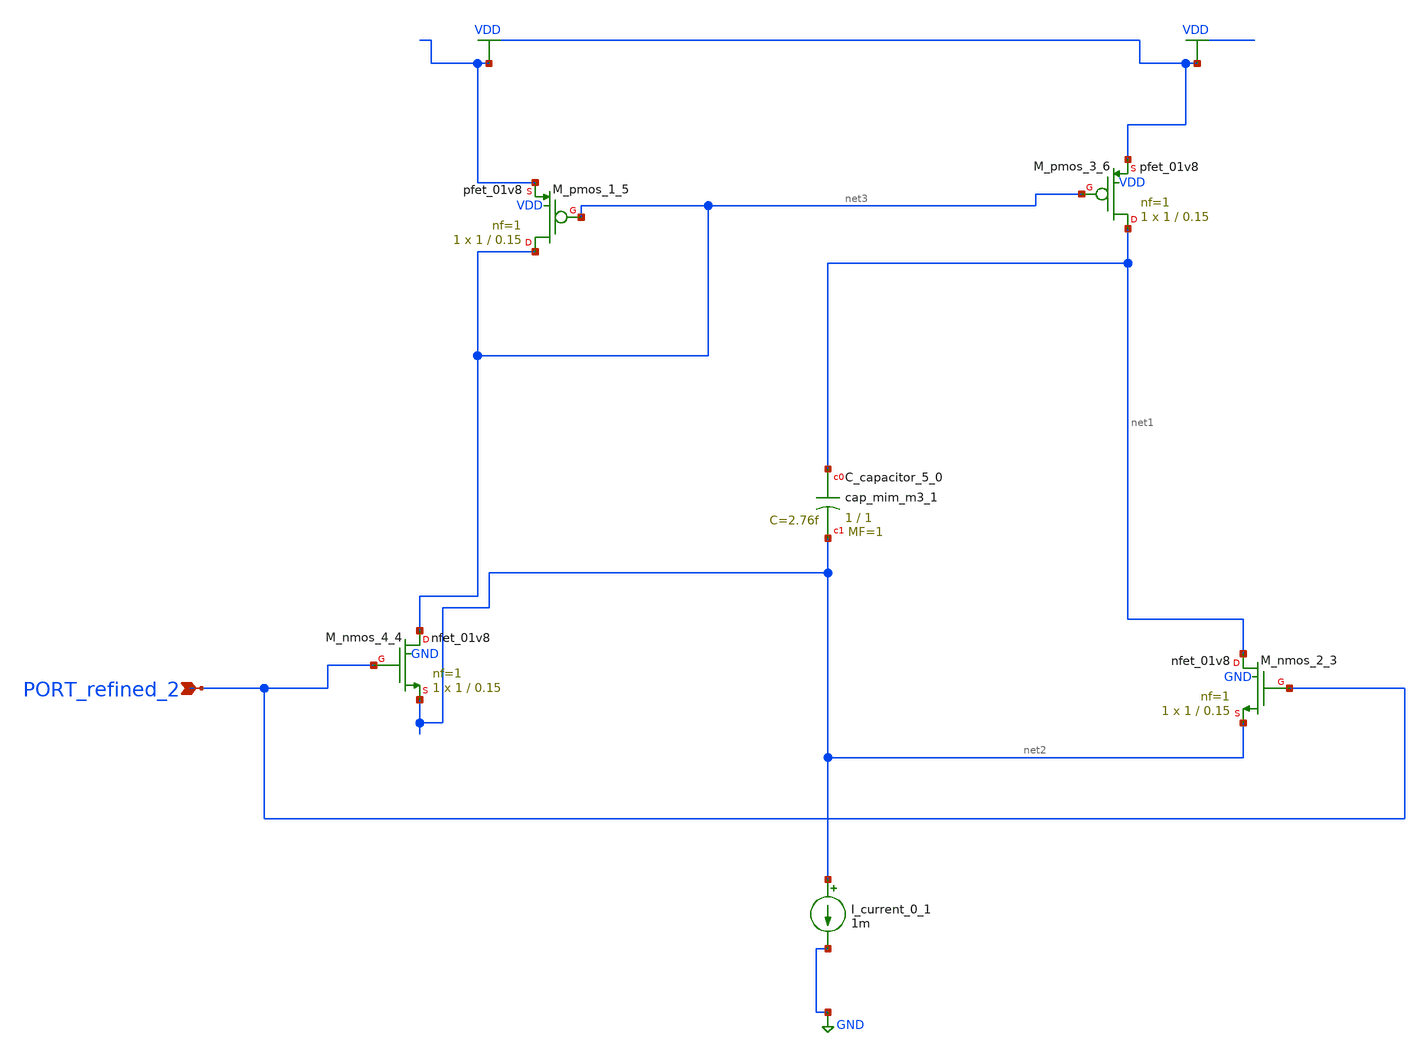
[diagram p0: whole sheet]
** sch_path: schematics/AMSNet/353.sch
**.subckt 353 PORT_refined_2
*.ipin PORT_refined_2
XC_capacitor_5_0 net1 net2 sky130_fd_pr__cap_mim_m3_1 W=1 L=1 MF=1 m=1
I_current_0_1 net2 GND 1m
XM_nmos_2_3 net1 PORT_refined_2 net2 GND sky130_fd_pr__nfet_01v8 L=0.15 W=1 nf=1 ad='int((1 + 1)/2) * 1 / 1 * 0.29'
+ as='int((1 + 2)/2) * 1 / 1 * 0.29' pd='2*int((1 + 1)/2) * (1 / 1 + 0.29)' ps='2*int((1 + 2)/2) * (1 / 1 + 0.29)'
+ nrd='0.29 / 1 ' nrs='0.29 / 1 ' sa=0 sb=0 sd=0 mult=1 m=1
XM_nmos_4_4 net3 PORT_refined_2 net2 GND sky130_fd_pr__nfet_01v8 L=0.15 W=1 nf=1 ad='int((1 + 1)/2) * 1 / 1 * 0.29'
+ as='int((1 + 2)/2) * 1 / 1 * 0.29' pd='2*int((1 + 1)/2) * (1 / 1 + 0.29)' ps='2*int((1 + 2)/2) * (1 / 1 + 0.29)'
+ nrd='0.29 / 1 ' nrs='0.29 / 1 ' sa=0 sb=0 sd=0 mult=1 m=1
XM_pmos_1_5 net3 net3 VDD VDD sky130_fd_pr__pfet_01v8 L=0.15 W=1 nf=1 ad='int((1 + 1)/2) * 1 / 1 * 0.29'
+ as='int((1 + 2)/2) * 1 / 1 * 0.29' pd='2*int((1 + 1)/2) * (1 / 1 + 0.29)' ps='2*int((1 + 2)/2) * (1 / 1 + 0.29)'
+ nrd='0.29 / 1 ' nrs='0.29 / 1 ' sa=0 sb=0 sd=0 mult=1 m=1
XM_pmos_3_6 net1 net3 VDD VDD sky130_fd_pr__pfet_01v8 L=0.15 W=1 nf=1 ad='int((1 + 1)/2) * 1 / 1 * 0.29'
+ as='int((1 + 2)/2) * 1 / 1 * 0.29' pd='2*int((1 + 1)/2) * (1 / 1 + 0.29)' ps='2*int((1 + 2)/2) * (1 / 1 + 0.29)'
+ nrd='0.29 / 1 ' nrs='0.29 / 1 ' sa=0 sb=0 sd=0 mult=1 m=1
**.ends
.GLOBAL GND
.GLOBAL VDD
.end
